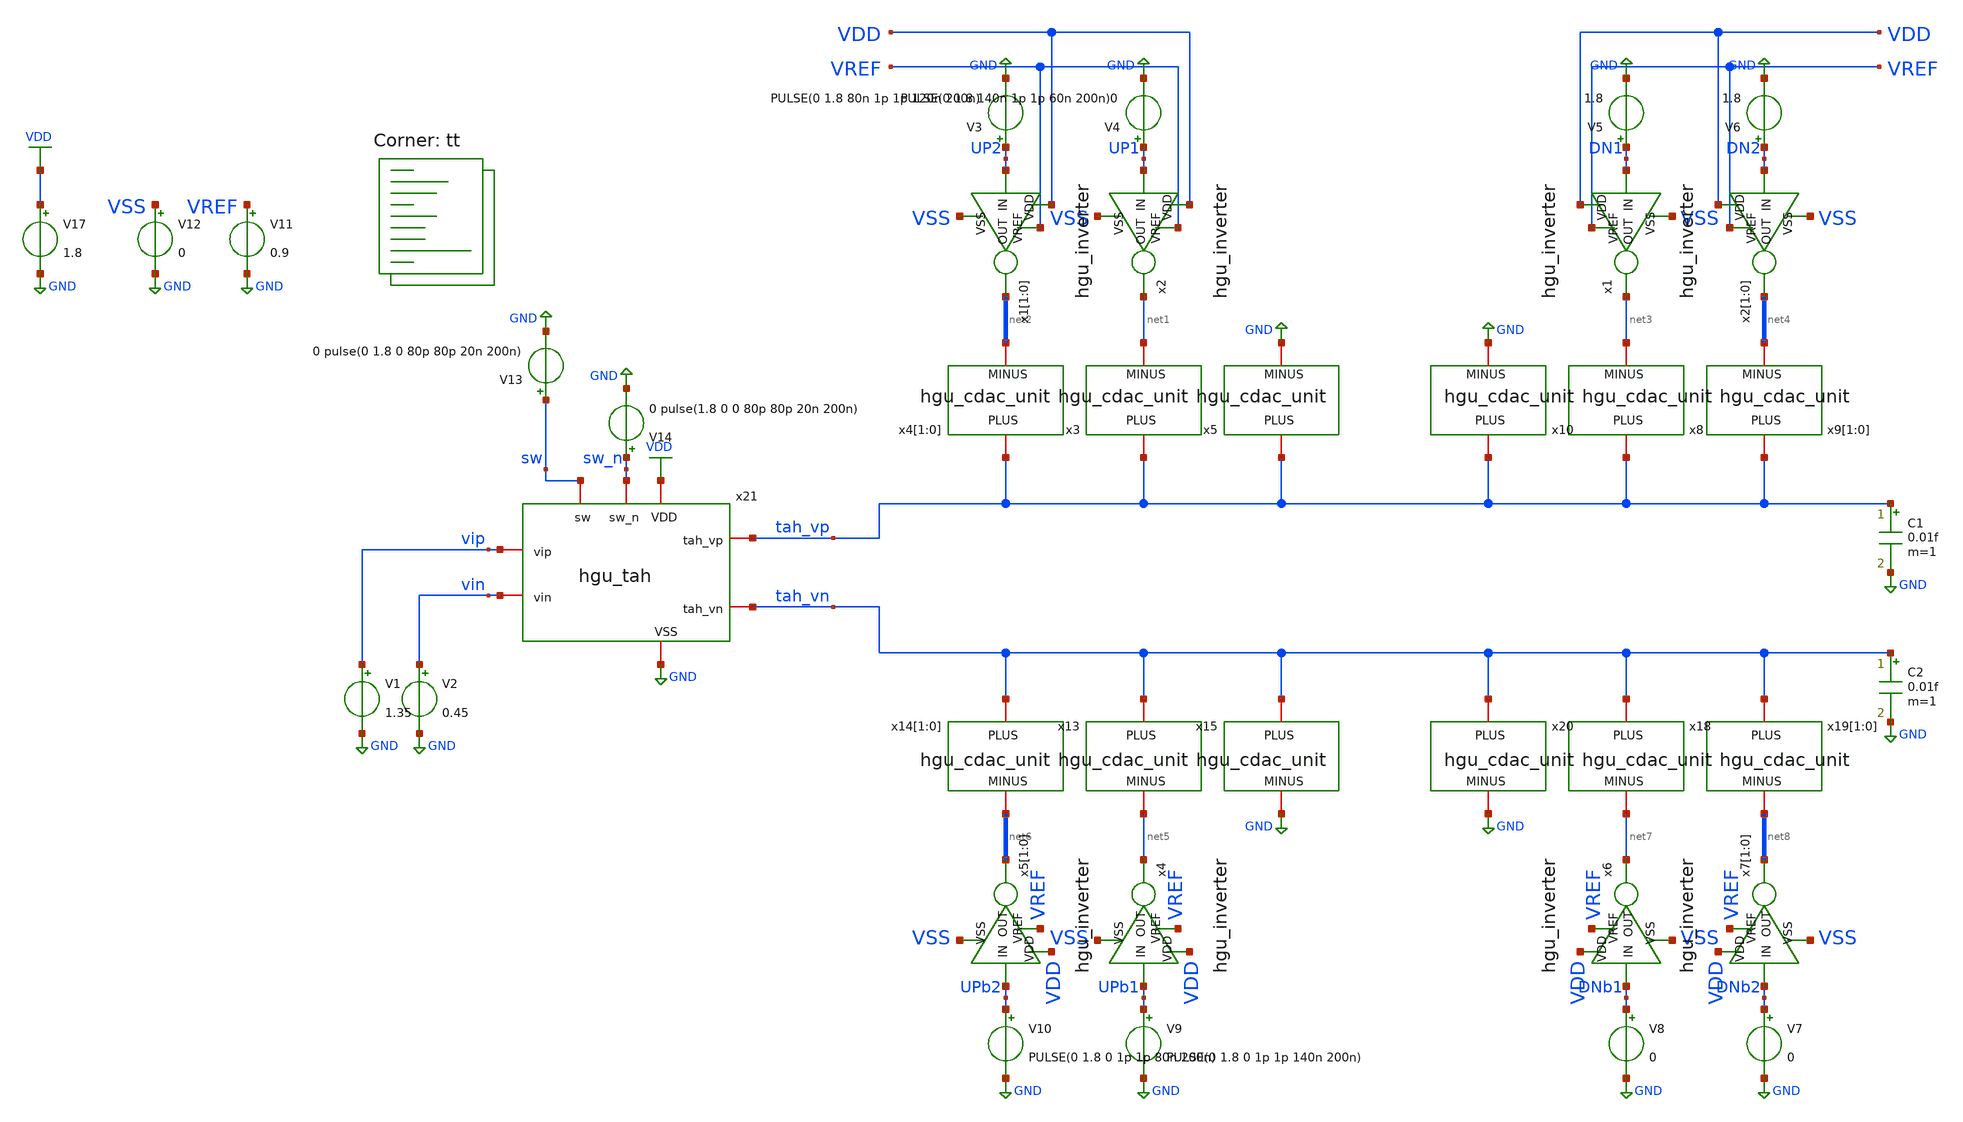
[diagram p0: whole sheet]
** sch_path: tb/tb_hgu_cdac_3bit.sch
**.subckt tb_hgu_cdac_3bit
x3 tah_vp net1 hgu_cdac_unit csize=1
x4[1] tah_vp net2[1] hgu_cdac_unit csize=1
x4[0] tah_vp net2[0] hgu_cdac_unit csize=1
x5 tah_vp GND hgu_cdac_unit csize=1
x8 tah_vp net3 hgu_cdac_unit csize=1
x9[1] tah_vp net4[1] hgu_cdac_unit csize=1
x9[0] tah_vp net4[0] hgu_cdac_unit csize=1
x10 tah_vp GND hgu_cdac_unit csize=1
x13 tah_vn net5 hgu_cdac_unit csize=1
x14[1] tah_vn net6[1] hgu_cdac_unit csize=1
x14[0] tah_vn net6[0] hgu_cdac_unit csize=1
x15 tah_vn GND hgu_cdac_unit csize=1
x18 tah_vn net7 hgu_cdac_unit csize=1
x19[1] tah_vn net8[1] hgu_cdac_unit csize=1
x19[0] tah_vn net8[0] hgu_cdac_unit csize=1
x20 tah_vn GND hgu_cdac_unit csize=1
C1 tah_vp GND 0.01f m=1
C2 tah_vn GND 0.01f m=1
V3 UP2 GND PULSE(0 1.8 80n 1p 1p 120n 200n)
V4 UP1 GND PULSE(0 1.8 140n 1p 1p 60n 200n)0
V5 DN1 GND 1.8
V6 DN2 GND 1.8
V7 DNb2 GND 0
V8 DNb1 GND 0
V9 UPb1 GND PULSE(0 1.8 0 1p 1p 140n 200n)
V10 UPb2 GND PULSE(0 1.8 0 1p 1p 80n 200n)
V11 VREF GND 0.9
V12 VSS GND 0
x21 sw VDD GND sw_n tah_vp vip vin tah_vn hgu_tah
V13 sw GND 0 pulse(0 1.8 0 80p 80p 20n 200n)
V14 sw_n GND 0 pulse(1.8 0 0 80p 80p 20n 200n)
V17 VDD GND 1.8
V1 vip GND 1.35
V2 vin GND 0.45
x2 VDD UP1 net1 VSS VREF hgu_inverter
x1[1] VDD UP2 net2[1] VSS VREF hgu_inverter
x1[0] VDD UP2 net2[0] VSS VREF hgu_inverter
x1 VDD DN1 net3 VSS VREF hgu_inverter
x2[1] VDD DN2 net4[1] VSS VREF hgu_inverter
x2[0] VDD DN2 net4[0] VSS VREF hgu_inverter
x4 VDD UPb1 net5 VSS VREF hgu_inverter
x5[1] VDD UPb2 net6[1] VSS VREF hgu_inverter
x5[0] VDD UPb2 net6[0] VSS VREF hgu_inverter
x6 VDD DNb1 net7 VSS VREF hgu_inverter
x7[1] VDD DNb2 net8[1] VSS VREF hgu_inverter
x7[0] VDD DNb2 net8[0] VSS VREF hgu_inverter
**** begin user architecture code


.save all
.temp = 25
.tran 100p 200n
.OPTIONS savecurrents

.control
	run
        plot v(up2)+14 v(up1)+12 v(dn2)+10 v(dn1)+8 v(upb2)+6 v(upb1)+4 v(dnb2)+2 v(dnb1)
	plot tah_vp-tah_vn vip-vin
.endc


.lib $::SKYWATER_MODELS/sky130.lib.spice tt
**** end user architecture code
**.ends
.GLOBAL GND
.GLOBAL VDD
.end
